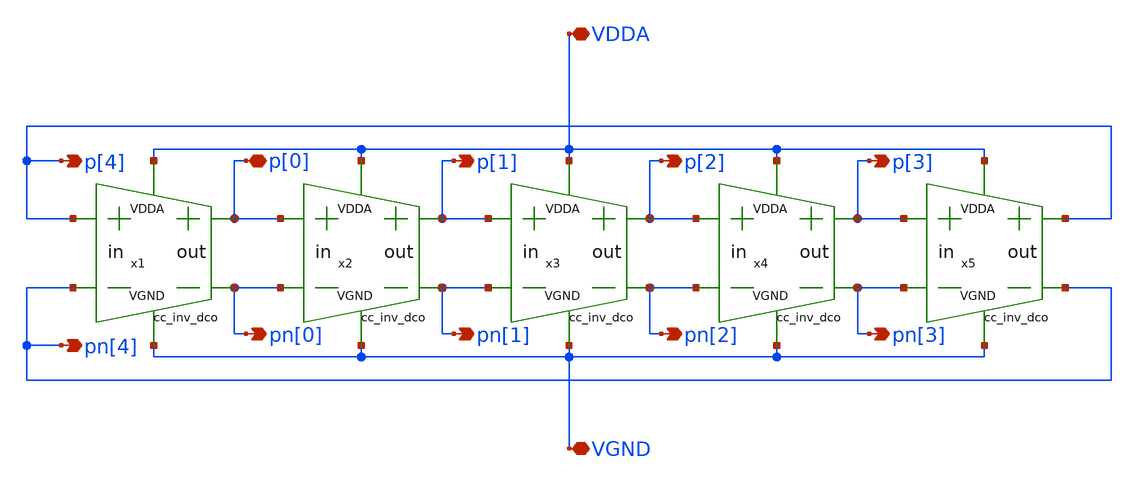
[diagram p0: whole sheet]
** sch_path: xschem/lib/5s_cc_osc_dco.sch
**.subckt 5s_cc_osc_dco VDDA VGND pn[0] p[0] pn[1] p[1] p[2] p[3] p[4] pn[2] pn[3] pn[4]
*.iopin VDDA
*.iopin VGND
*.opin pn[0]
*.iopin p[0]
*.opin pn[1]
*.opin p[1]
*.opin p[2]
*.opin p[3]
*.opin p[4]
*.opin pn[2]
*.opin pn[3]
*.opin pn[4]
x1 VDDA p[0] p[4] pn[4] pn[0] VGND cc_inv_dco
x2 VDDA p[1] p[0] pn[0] pn[1] VGND cc_inv_dco
x3 VDDA p[2] p[1] pn[1] pn[2] VGND cc_inv_dco
x4 VDDA p[3] p[2] pn[2] pn[3] VGND cc_inv_dco
x5 VDDA p[4] p[3] pn[3] pn[4] VGND cc_inv_dco
**.ends

* expanding   symbol:  ../lib/cc_inv_dco.sym # of pins=6
** sym_path: xschem/lib/cc_inv_dco.sym
** sch_path: xschem/lib/cc_inv_dco.sch
.subckt cc_inv_dco VDDA outp inp inn outn VGND
*.opin outp
*.ipin inn
*.iopin VGND
*.opin outn
*.ipin inp
*.iopin VDDA
x1 VDDA VGND outp inp main_inv_dco
x2 VPWR VGND outn inn main_inv_dco
x3 outp outn VDDA VGND aux_inv_dco
x4 outn outp VDDA VGND aux_inv_dco
.ends


* expanding   symbol:  ../lib/main_inv_dco.sym # of pins=4
** sym_path: xschem/lib/main_inv_dco.sym
** sch_path: xschem/lib/main_inv_dco.sch
.subckt main_inv_dco VDDA VGND Y A
*.iopin VDDA
*.iopin VGND
*.ipin A
*.opin Y
XM3 Y A VGND VGND sky130_fd_pr__nfet_01v8 L=1.2 W=4 nf=2 ad='int((nf+1)/2) * W/nf * 0.29' as='int((nf+2)/2) * W/nf * 0.29'
+ pd='2*int((nf+1)/2) * (W/nf + 0.29)' ps='2*int((nf+2)/2) * (W/nf + 0.29)' nrd='0.29 / W' nrs='0.29 / W'
+ sa=0 sb=0 sd=0 mult=1 m=1
XM2 Y A VDDA VDDA sky130_fd_pr__pfet_01v8 L=1.2 W=6 nf=2 ad='int((nf+1)/2) * W/nf * 0.29' as='int((nf+2)/2) * W/nf * 0.29'
+ pd='2*int((nf+1)/2) * (W/nf + 0.29)' ps='2*int((nf+2)/2) * (W/nf + 0.29)' nrd='0.29 / W' nrs='0.29 / W'
+ sa=0 sb=0 sd=0 mult=1 m=1
.ends


* expanding   symbol:  ../lib/aux_inv_dco.sym # of pins=4
** sym_path: xschem/lib/aux_inv_dco.sym
** sch_path: xschem/lib/aux_inv_dco.sch
.subckt aux_inv_dco A Y VDDA VGND
*.iopin VDDA
*.iopin VGND
*.ipin A
*.opin Y
XM3 Y A VGND VGND sky130_fd_pr__nfet_01v8 L=1.2 W=2 nf=1 ad='int((nf+1)/2) * W/nf * 0.29' as='int((nf+2)/2) * W/nf * 0.29'
+ pd='2*int((nf+1)/2) * (W/nf + 0.29)' ps='2*int((nf+2)/2) * (W/nf + 0.29)' nrd='0.29 / W' nrs='0.29 / W'
+ sa=0 sb=0 sd=0 mult=1 m=1
XM2 Y A VDDA VDDA sky130_fd_pr__pfet_01v8 L=1.2 W=3 nf=1 ad='int((nf+1)/2) * W/nf * 0.29' as='int((nf+2)/2) * W/nf * 0.29'
+ pd='2*int((nf+1)/2) * (W/nf + 0.29)' ps='2*int((nf+2)/2) * (W/nf + 0.29)' nrd='0.29 / W' nrs='0.29 / W'
+ sa=0 sb=0 sd=0 mult=1 m=1
.ends

.end
